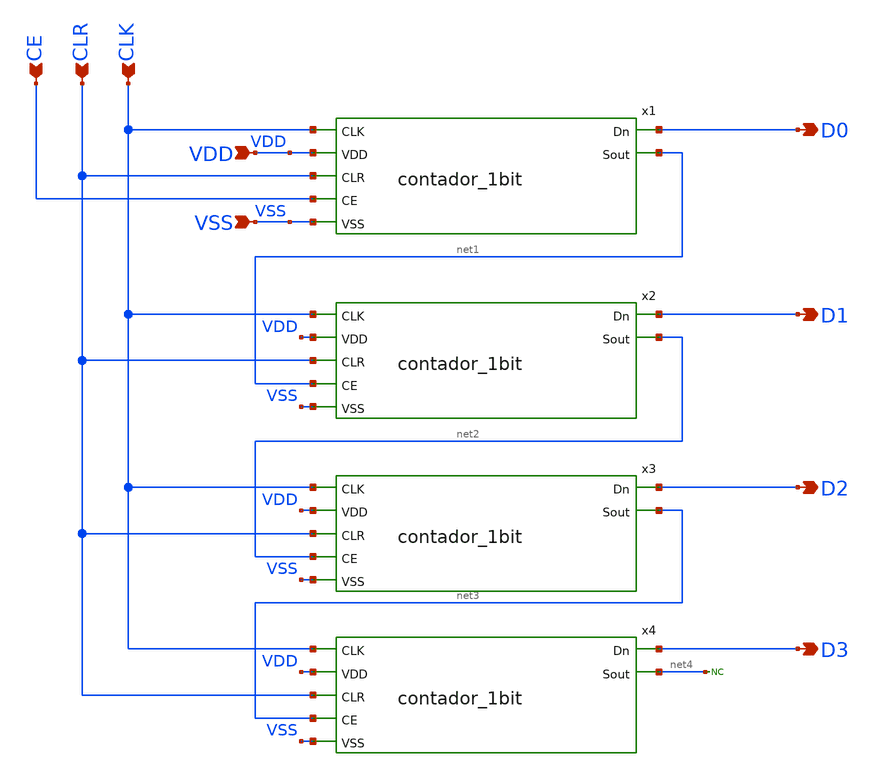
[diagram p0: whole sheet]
** sch_path: icdesign/sch/Contador4bit/contador_4bit.sch
**.subckt contador_4bit CLR CLK VDD VSS CE D0 D1 D2 D3
*.ipin CLR
*.ipin CLK
*.ipin VDD
*.ipin VSS
*.ipin CE
*.opin D0
*.opin D1
*.opin D2
*.opin D3
x1 D0 CLK VDD CLR CE VSS net1 contador_1bit
x2 D1 CLK VDD CLR net1 VSS net2 contador_1bit
x3 D2 CLK VDD CLR net2 VSS net3 contador_1bit
x4 D3 CLK VDD CLR net3 VSS net4 contador_1bit
* noconn #net4
**.ends
.end
